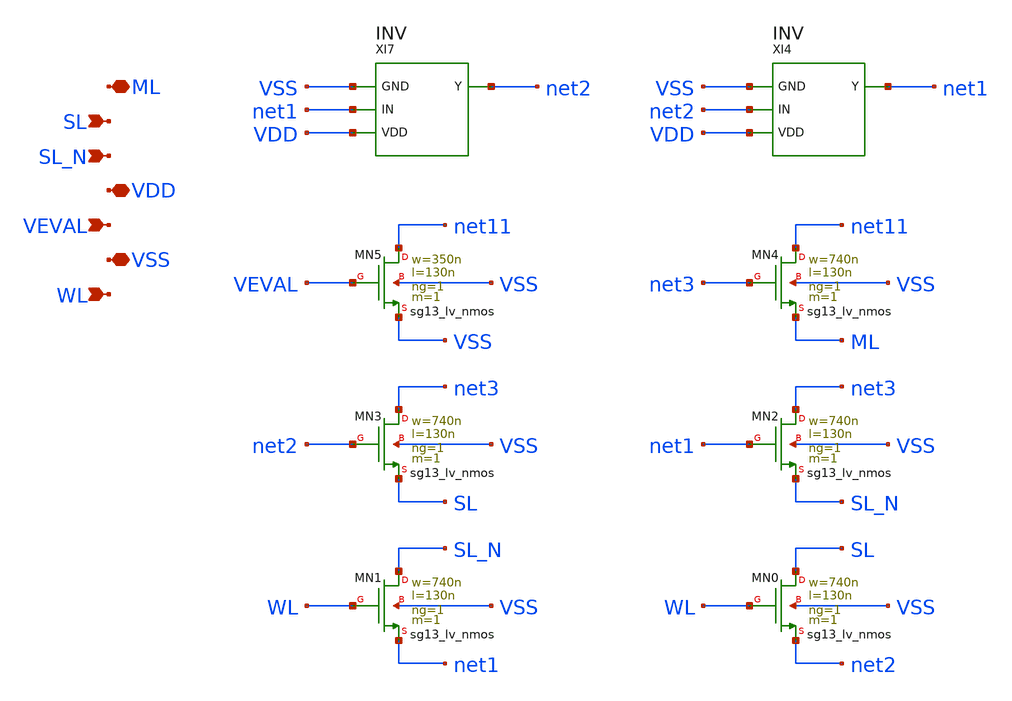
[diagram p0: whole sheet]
** sch_path: SoC6169-main/schematic/xschem/CELL.sch
* Copyright 2026 USFQ CAM team
* Licensed under the Apache License, Version 2.0 (the "License");
* you may not use this file except in compliance with the License.
* You may obtain a copy of the License at
* https://www.apache.org/licenses/LICENSE-2.0
* Unless required by applicable law or agreed to in writing, software
* distributed under the License is distributed on an "AS IS" BASIS,
* WITHOUT WARRANTIES OR CONDITIONS OF ANY KIND, either express or implied.
* See the License for the specific language governing permissions and
* limitations under the License.
**.subckt CELL ML SL SL_N VDD VEVAL VSS WL
*.iopin ML
*.ipin SL
*.ipin SL_N
*.iopin VDD
*.ipin VEVAL
*.iopin VSS
*.ipin WL
XI7 VSS net1 VDD net2 INV
XI4 VSS net2 VDD net1 INV
XMN5 net11 VEVAL VSS VSS sg13_lv_nmos w=350n l=130n ng=1 m=1 mm_ok=1
XMN4 net11 net3 ML VSS sg13_lv_nmos w=740n l=130n ng=1 m=1 mm_ok=1
XMN3 net3 net2 SL VSS sg13_lv_nmos w=740n l=130n ng=1 m=1 mm_ok=1
XMN2 net3 net1 SL_N VSS sg13_lv_nmos w=740n l=130n ng=1 m=1 mm_ok=1
XMN1 SL_N WL net1 VSS sg13_lv_nmos w=740n l=130n ng=1 m=1 mm_ok=1
XMN0 SL WL net2 VSS sg13_lv_nmos w=740n l=130n ng=1 m=1 mm_ok=1
**.ends

* expanding   symbol:  INV.sym # of pins=4
** sym_path: SoC6169-main/schematic/xschem/INV.sym
** sch_path: SoC6169-main/schematic/xschem/INV.sch
.subckt INV GND IN VDD Y
*.iopin GND
*.ipin IN
*.iopin VDD
*.opin Y
XMN0 Y IN GND GND sg13_lv_nmos w=200n l=130n ng=1 m=1 mm_ok=1
XMP0 Y IN VDD VDD sg13_lv_pmos w=400n l=130n ng=1 m=1 mm_ok=1
.ends

.end
